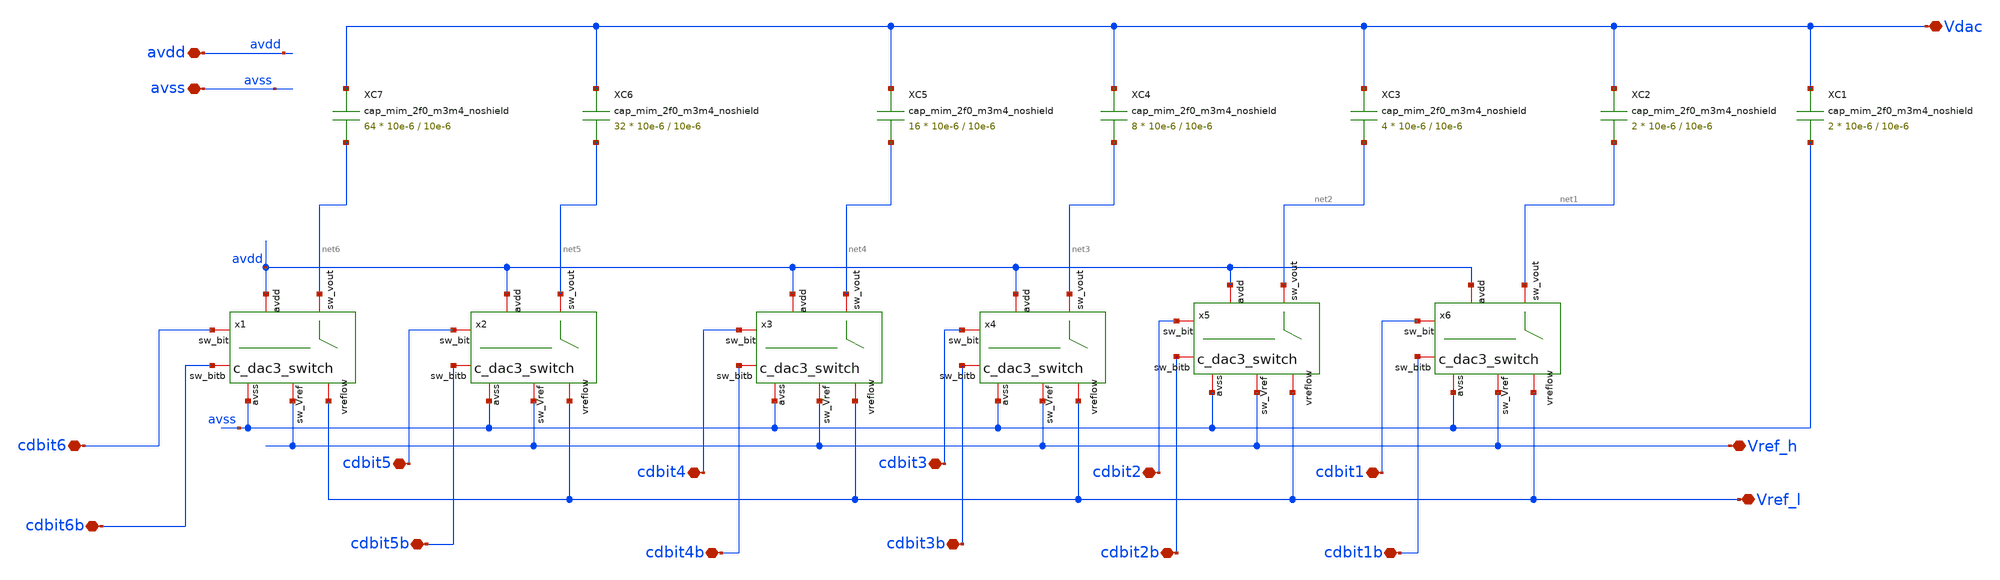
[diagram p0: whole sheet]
** sch_path: designs/libs/WK_Kadam/CDAC_V3.sch
**.subckt CDAC_V3 Vref_h Vdac avdd avss cdbit6 cdbit5 cdbit4 cdbit3 cdbit2 cdbit1 Vref_l cdbit6b
*+ cdbit5b cdbit4b cdbit3b cdbit2b cdbit1b
*.iopin Vref_h
*.iopin Vdac
*.iopin avdd
*.iopin avss
*.iopin cdbit6
*.iopin cdbit5
*.iopin cdbit4
*.iopin cdbit3
*.iopin cdbit2
*.iopin cdbit1
*.iopin Vref_l
*.iopin cdbit6b
*.iopin cdbit5b
*.iopin cdbit4b
*.iopin cdbit3b
*.iopin cdbit2b
*.iopin cdbit1b
XC3 Vdac net2 cap_mim_2f0_m3m4_noshield c_width=10e-6 c_length=10e-6 m=4
XC4 Vdac net3 cap_mim_2f0_m3m4_noshield c_width=10e-6 c_length=10e-6 m=8
XC5 Vdac net4 cap_mim_2f0_m3m4_noshield c_width=10e-6 c_length=10e-6 m=16
XC6 Vdac net5 cap_mim_2f0_m3m4_noshield c_width=10e-6 c_length=10e-6 m=32
XC7 Vdac net6 cap_mim_2f0_m3m4_noshield c_width=10e-6 c_length=10e-6 m=64
XC1 Vdac avss cap_mim_2f0_m3m4_noshield c_width=10e-6 c_length=10e-6 m=2
XC2 Vdac net1 cap_mim_2f0_m3m4_noshield c_width=10e-6 c_length=10e-6 m=2
x1 net6 cdbit6 avss avdd Vref_h Vref_l cdbit6b c_dac3_switch
x2 net5 cdbit5 avss avdd Vref_h Vref_l cdbit5b c_dac3_switch
x3 net4 cdbit4 avss avdd Vref_h Vref_l cdbit4b c_dac3_switch
x4 net3 cdbit3 avss avdd Vref_h Vref_l cdbit3b c_dac3_switch
x5 net2 cdbit2 avss avdd Vref_h Vref_l cdbit2b c_dac3_switch
x6 net1 cdbit1 avss avdd Vref_h Vref_l cdbit1b c_dac3_switch
**.ends
.end
